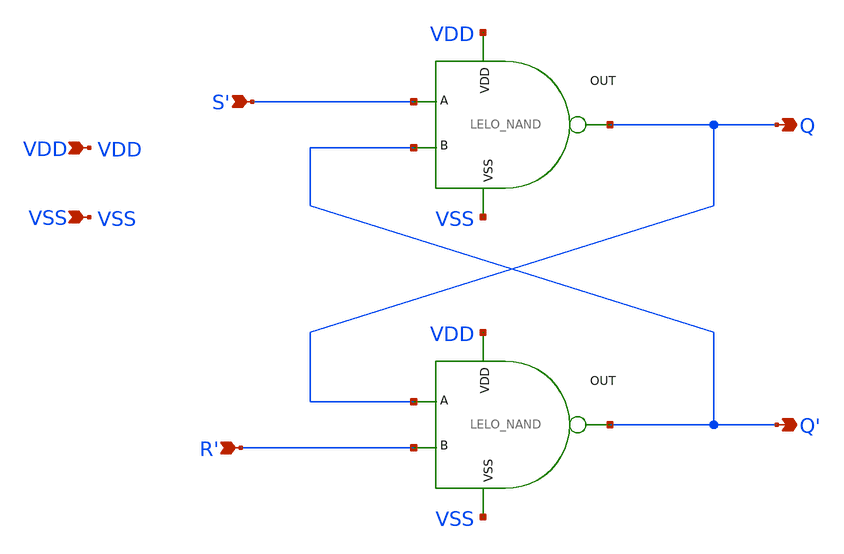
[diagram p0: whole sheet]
** sch_path: design/LELO_SVOD_SKY130A/LELO_SR_LATCH_.sch
**.subckt LELO_SR_LATCH_ S' R' VDD VSS Q Q'
*.ipin S'
*.ipin R'
*.ipin VDD
*.ipin VSS
*.opin Q
*.opin Q'
x1 VDD Q S' Q' VSS LELO_NAND
x2 VDD Q' Q R' VSS LELO_NAND
**.ends

* expanding   symbol:  LELO_SVOD_SKY130A/LELO_NAND.sym # of pins=5
** sym_path: design/LELO_SVOD_SKY130A/LELO_NAND.sym
** sch_path: design/LELO_SVOD_SKY130A/LELO_NAND.sch
.subckt LELO_NAND VDD OUT A B VSS
*.ipin VDD
*.ipin VSS
*.opin OUT
*.ipin A
*.ipin B
XM1 OUT B net1 net1 sky130_fd_pr__nfet_01v8 L=0.15 W=0.42 nf=1 ad='int((1 + 1)/2) * 0.42 / 1 * 0.29'
+ as='int((1 + 2)/2) * 0.42 / 1 * 0.29' pd='2*int((1 + 1)/2) * (0.42 / 1 + 0.29)' ps='2*int((1 + 2)/2) * (0.42 / 1 + 0.29)'
+ nrd='0.29 / 0.42 ' nrs='0.29 / 0.42 ' sa=0 sb=0 sd=0 mult=1 m=1
XM2 net1 A VSS VSS sky130_fd_pr__nfet_01v8 L=0.15 W=0.42 nf=1 ad='int((1 + 1)/2) * 0.42 / 1 * 0.29' as='int((1 + 2)/2) * 0.42 / 1 * 0.29'
+ pd='2*int((1 + 1)/2) * (0.42 / 1 + 0.29)' ps='2*int((1 + 2)/2) * (0.42 / 1 + 0.29)' nrd='0.29 / 0.42 '
+ nrs='0.29 / 0.42 ' sa=0 sb=0 sd=0 mult=1 m=1
XM3 OUT A VDD VDD sky130_fd_pr__pfet_01v8_hvt L=0.15 W=0.42 nf=1 ad='int((1 + 1)/2) * 0.42 / 1 * 0.29'
+ as='int((1 + 2)/2) * 0.42 / 1 * 0.29' pd='2*int((1 + 1)/2) * (0.42 / 1 + 0.29)' ps='2*int((1 + 2)/2) * (0.42 / 1 + 0.29)'
+ nrd='0.29 / 0.42 ' nrs='0.29 / 0.42 ' sa=0 sb=0 sd=0 mult=1 m=1
XM4 OUT B VDD VDD sky130_fd_pr__pfet_01v8_hvt L=0.15 W=0.42 nf=1 ad='int((1 + 1)/2) * 0.42 / 1 * 0.29'
+ as='int((1 + 2)/2) * 0.42 / 1 * 0.29' pd='2*int((1 + 1)/2) * (0.42 / 1 + 0.29)' ps='2*int((1 + 2)/2) * (0.42 / 1 + 0.29)'
+ nrd='0.29 / 0.42 ' nrs='0.29 / 0.42 ' sa=0 sb=0 sd=0 mult=1 m=1
.ends

.end
